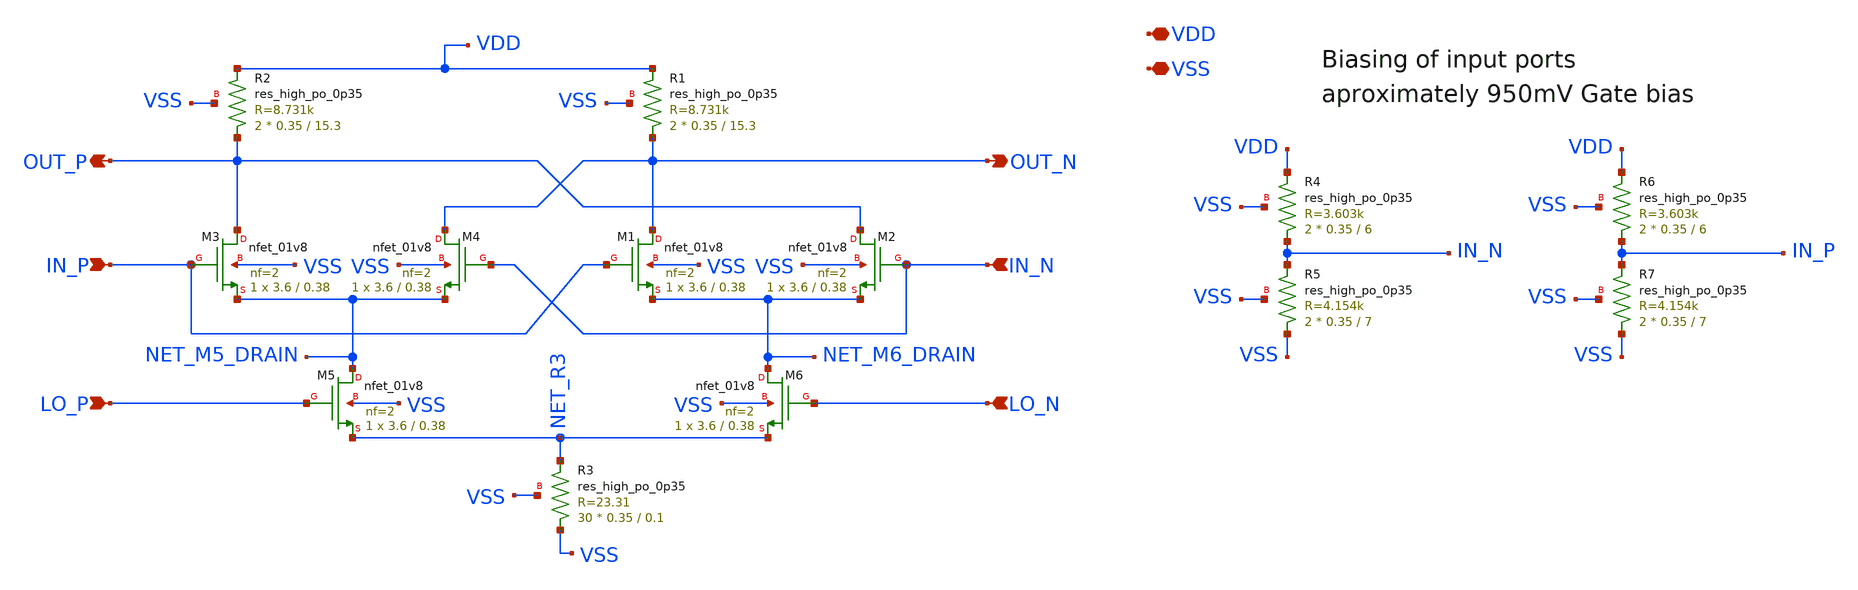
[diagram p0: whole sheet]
** sch_path: xschem/gilbert_mixer.sch
**.subckt gilbert_mixer LO_P LO_N IN_P IN_N OUT_N OUT_P VDD VSS
*.ipin LO_P
*.ipin LO_N
*.ipin IN_P
*.ipin IN_N
*.opin OUT_N
*.opin OUT_P
*.iopin VDD
*.iopin VSS
XR3 VSS NET_R3 VSS sky130_fd_pr__res_high_po_0p35 L=0.1 mult=30 m=30
XM2 OUT_P IN_N NET_M6_DRAIN VSS sky130_fd_pr__nfet_01v8 L=0.38 W=3.6 nf=2 ad='int((nf+1)/2) * W/nf * 0.29'
+ as='int((nf+2)/2) * W/nf * 0.29' pd='2*int((nf+1)/2) * (W/nf + 0.29)' ps='2*int((nf+2)/2) * (W/nf + 0.29)'
+ nrd='0.29 / W' nrs='0.29 / W' sa=0 sb=0 sd=0 mult=1 m=1
XM4 OUT_N IN_N NET_M5_DRAIN VSS sky130_fd_pr__nfet_01v8 L=0.38 W=3.6 nf=2 ad='int((nf+1)/2) * W/nf * 0.29'
+ as='int((nf+2)/2) * W/nf * 0.29' pd='2*int((nf+1)/2) * (W/nf + 0.29)' ps='2*int((nf+2)/2) * (W/nf + 0.29)'
+ nrd='0.29 / W' nrs='0.29 / W' sa=0 sb=0 sd=0 mult=1 m=1
XM6 NET_M6_DRAIN LO_N NET_R3 VSS sky130_fd_pr__nfet_01v8 L=0.38 W=3.6 nf=2 ad='int((nf+1)/2) * W/nf * 0.29'
+ as='int((nf+2)/2) * W/nf * 0.29' pd='2*int((nf+1)/2) * (W/nf + 0.29)' ps='2*int((nf+2)/2) * (W/nf + 0.29)'
+ nrd='0.29 / W' nrs='0.29 / W' sa=0 sb=0 sd=0 mult=1 m=1
XM1 OUT_N IN_P NET_M6_DRAIN VSS sky130_fd_pr__nfet_01v8 L=0.38 W=3.6 nf=2 ad='int((nf+1)/2) * W/nf * 0.29'
+ as='int((nf+2)/2) * W/nf * 0.29' pd='2*int((nf+1)/2) * (W/nf + 0.29)' ps='2*int((nf+2)/2) * (W/nf + 0.29)'
+ nrd='0.29 / W' nrs='0.29 / W' sa=0 sb=0 sd=0 mult=1 m=1
XM3 OUT_P IN_P NET_M5_DRAIN VSS sky130_fd_pr__nfet_01v8 L=0.38 W=3.6 nf=2 ad='int((nf+1)/2) * W/nf * 0.29'
+ as='int((nf+2)/2) * W/nf * 0.29' pd='2*int((nf+1)/2) * (W/nf + 0.29)' ps='2*int((nf+2)/2) * (W/nf + 0.29)'
+ nrd='0.29 / W' nrs='0.29 / W' sa=0 sb=0 sd=0 mult=1 m=1
XM5 NET_M5_DRAIN LO_P NET_R3 VSS sky130_fd_pr__nfet_01v8 L=0.38 W=3.6 nf=2 ad='int((nf+1)/2) * W/nf * 0.29'
+ as='int((nf+2)/2) * W/nf * 0.29' pd='2*int((nf+1)/2) * (W/nf + 0.29)' ps='2*int((nf+2)/2) * (W/nf + 0.29)'
+ nrd='0.29 / W' nrs='0.29 / W' sa=0 sb=0 sd=0 mult=1 m=1
XR1 OUT_N VDD VSS sky130_fd_pr__res_high_po_0p35 L=15.3 mult=2 m=2
XR2 OUT_P VDD VSS sky130_fd_pr__res_high_po_0p35 L=15.3 mult=2 m=2
XR4 IN_N VDD VSS sky130_fd_pr__res_high_po_0p35 L=6 mult=2 m=2
XR5 VSS IN_N VSS sky130_fd_pr__res_high_po_0p35 L=7 mult=2 m=2
XR6 IN_P VDD VSS sky130_fd_pr__res_high_po_0p35 L=6 mult=2 m=2
XR7 VSS IN_P VSS sky130_fd_pr__res_high_po_0p35 L=7 mult=2 m=2
**.ends
.end
